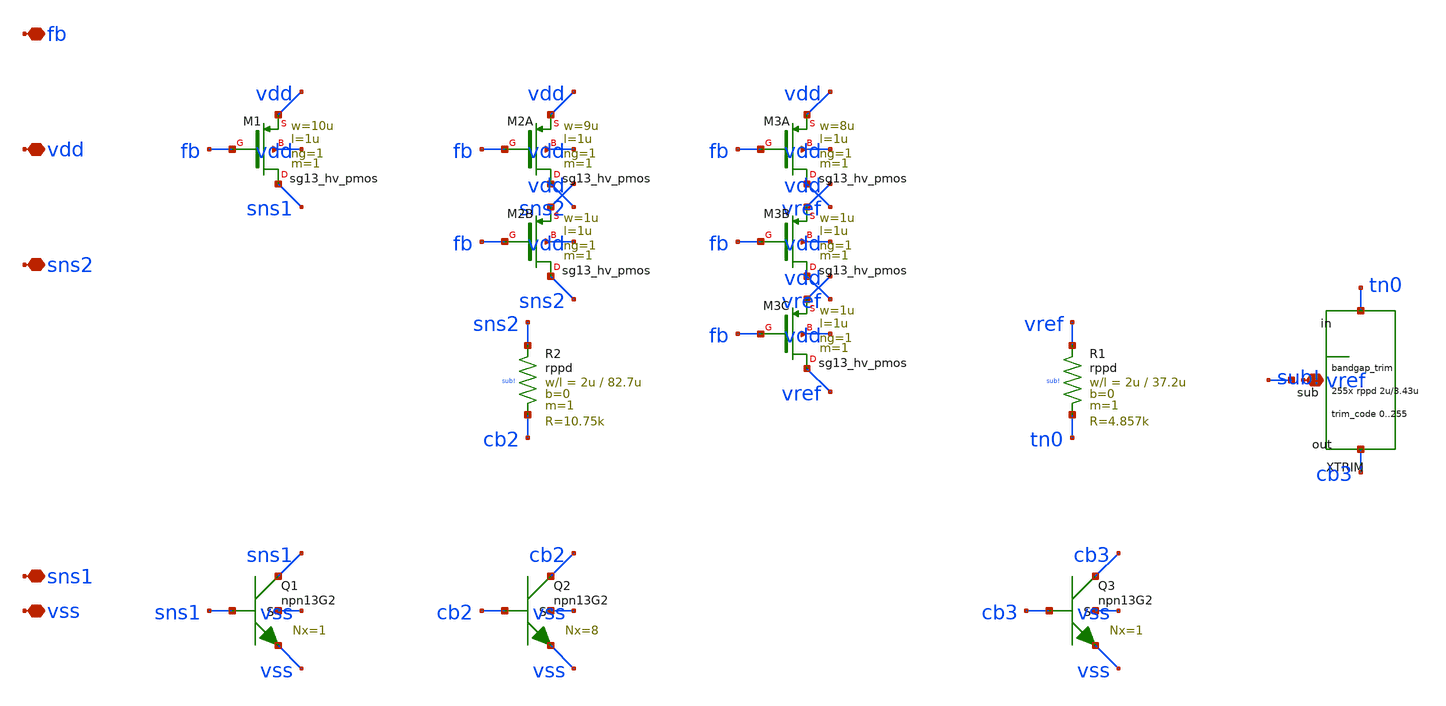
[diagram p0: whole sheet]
** sch_path: design/bandgap_core.sch
**.subckt bandgap_core vdd vss fb sns1 sns2 vref
*.iopin vdd
*.iopin vss
*.iopin fb
*.iopin sns1
*.iopin sns2
*.iopin vref
XM1 sns1 fb vdd vdd sg13_hv_pmos w=10u l=1u ng=1 m=1 mm_ok=1
XQ1 sns1 sns1 vss vss npn13G2 Nx=1 mm_ok=1
XM2A sns2 fb vdd vdd sg13_hv_pmos w=9u l=1u ng=1 m=1 mm_ok=1
XM2B sns2 fb vdd vdd sg13_hv_pmos w=1u l=1u ng=1 m=1 mm_ok=1
XR2 sns2 cb2 sub! rppd w=2u l=82.7u m=1 b=0 mm_ok=1
XQ2 cb2 cb2 vss vss npn13G2 Nx=8 mm_ok=1
XM3A vref fb vdd vdd sg13_hv_pmos w=8u l=1u ng=1 m=1 mm_ok=1
XM3B vref fb vdd vdd sg13_hv_pmos w=1u l=1u ng=1 m=1 mm_ok=1
XM3C vref fb vdd vdd sg13_hv_pmos w=1u l=1u ng=1 m=1 mm_ok=1
XR1 vref tn0 sub! rppd w=2u l=37.2u m=1 b=0 mm_ok=1
XXTRIM tn0 cb3 sub! bandgap_trim
XQ3 cb3 cb3 vss vss npn13G2 Nx=1 mm_ok=1
**.ends

* expanding   symbol:  bandgap_trim.sym # of pins=3
** sym_path: design/bandgap_trim.sym
** sch_path: design/bandgap_trim.sch
.subckt bandgap_trim in out sub

*.iopin in
*.iopin out
*.iopin sub
XRU1 in t001 sub rppd w=2u l=3.43u m=1 b=0 mm_ok=1
XRU2 t001 t002 sub rppd w=2u l=3.43u m=1 b=0 mm_ok=1
XRU3 t002 t003 sub rppd w=2u l=3.43u m=1 b=0 mm_ok=1
XRU4 t003 t004 sub rppd w=2u l=3.43u m=1 b=0 mm_ok=1
XRU5 t004 t005 sub rppd w=2u l=3.43u m=1 b=0 mm_ok=1
XRU6 t005 t006 sub rppd w=2u l=3.43u m=1 b=0 mm_ok=1
XRU7 t006 t007 sub rppd w=2u l=3.43u m=1 b=0 mm_ok=1
XRU8 t007 t008 sub rppd w=2u l=3.43u m=1 b=0 mm_ok=1
XRU9 t008 t009 sub rppd w=2u l=3.43u m=1 b=0 mm_ok=1
XRU10 t009 t010 sub rppd w=2u l=3.43u m=1 b=0 mm_ok=1
XRU11 t010 t011 sub rppd w=2u l=3.43u m=1 b=0 mm_ok=1
XRU12 t011 t012 sub rppd w=2u l=3.43u m=1 b=0 mm_ok=1
XRU13 t012 t013 sub rppd w=2u l=3.43u m=1 b=0 mm_ok=1
XRU14 t013 t014 sub rppd w=2u l=3.43u m=1 b=0 mm_ok=1
XRU15 t014 t015 sub rppd w=2u l=3.43u m=1 b=0 mm_ok=1
XRU16 t015 t016 sub rppd w=2u l=3.43u m=1 b=0 mm_ok=1
XRU17 t016 t017 sub rppd w=2u l=3.43u m=1 b=0 mm_ok=1
XRU18 t017 t018 sub rppd w=2u l=3.43u m=1 b=0 mm_ok=1
XRU19 t018 t019 sub rppd w=2u l=3.43u m=1 b=0 mm_ok=1
XRU20 t019 t020 sub rppd w=2u l=3.43u m=1 b=0 mm_ok=1
XRU21 t020 t021 sub rppd w=2u l=3.43u m=1 b=0 mm_ok=1
XRU22 t021 t022 sub rppd w=2u l=3.43u m=1 b=0 mm_ok=1
XRU23 t022 t023 sub rppd w=2u l=3.43u m=1 b=0 mm_ok=1
XRU24 t023 t024 sub rppd w=2u l=3.43u m=1 b=0 mm_ok=1
XRU25 t024 t025 sub rppd w=2u l=3.43u m=1 b=0 mm_ok=1
XRU26 t025 t026 sub rppd w=2u l=3.43u m=1 b=0 mm_ok=1
XRU27 t026 t027 sub rppd w=2u l=3.43u m=1 b=0 mm_ok=1
XRU28 t027 t028 sub rppd w=2u l=3.43u m=1 b=0 mm_ok=1
XRU29 t028 t029 sub rppd w=2u l=3.43u m=1 b=0 mm_ok=1
XRU30 t029 t030 sub rppd w=2u l=3.43u m=1 b=0 mm_ok=1
XRU31 t030 t031 sub rppd w=2u l=3.43u m=1 b=0 mm_ok=1
XRU32 t031 t032 sub rppd w=2u l=3.43u m=1 b=0 mm_ok=1
XRU33 t032 t033 sub rppd w=2u l=3.43u m=1 b=0 mm_ok=1
XRU34 t033 t034 sub rppd w=2u l=3.43u m=1 b=0 mm_ok=1
XRU35 t034 t035 sub rppd w=2u l=3.43u m=1 b=0 mm_ok=1
XRU36 t035 t036 sub rppd w=2u l=3.43u m=1 b=0 mm_ok=1
XRU37 t036 t037 sub rppd w=2u l=3.43u m=1 b=0 mm_ok=1
XRU38 t037 t038 sub rppd w=2u l=3.43u m=1 b=0 mm_ok=1
XRU39 t038 t039 sub rppd w=2u l=3.43u m=1 b=0 mm_ok=1
XRU40 t039 t040 sub rppd w=2u l=3.43u m=1 b=0 mm_ok=1
XRU41 t040 t041 sub rppd w=2u l=3.43u m=1 b=0 mm_ok=1
XRU42 t041 t042 sub rppd w=2u l=3.43u m=1 b=0 mm_ok=1
XRU43 t042 t043 sub rppd w=2u l=3.43u m=1 b=0 mm_ok=1
XRU44 t043 t044 sub rppd w=2u l=3.43u m=1 b=0 mm_ok=1
XRU45 t044 t045 sub rppd w=2u l=3.43u m=1 b=0 mm_ok=1
XRU46 t045 t046 sub rppd w=2u l=3.43u m=1 b=0 mm_ok=1
XRU47 t046 t047 sub rppd w=2u l=3.43u m=1 b=0 mm_ok=1
XRU48 t047 t048 sub rppd w=2u l=3.43u m=1 b=0 mm_ok=1
XRU49 t048 t049 sub rppd w=2u l=3.43u m=1 b=0 mm_ok=1
XRU50 t049 t050 sub rppd w=2u l=3.43u m=1 b=0 mm_ok=1
XRU51 t050 t051 sub rppd w=2u l=3.43u m=1 b=0 mm_ok=1
XRU52 t051 t052 sub rppd w=2u l=3.43u m=1 b=0 mm_ok=1
XRU53 t052 t053 sub rppd w=2u l=3.43u m=1 b=0 mm_ok=1
XRU54 t053 t054 sub rppd w=2u l=3.43u m=1 b=0 mm_ok=1
XRU55 t054 t055 sub rppd w=2u l=3.43u m=1 b=0 mm_ok=1
XRU56 t055 t056 sub rppd w=2u l=3.43u m=1 b=0 mm_ok=1
XRU57 t056 t057 sub rppd w=2u l=3.43u m=1 b=0 mm_ok=1
XRU58 t057 t058 sub rppd w=2u l=3.43u m=1 b=0 mm_ok=1
XRU59 t058 t059 sub rppd w=2u l=3.43u m=1 b=0 mm_ok=1
XRU60 t059 t060 sub rppd w=2u l=3.43u m=1 b=0 mm_ok=1
XRU61 t060 t061 sub rppd w=2u l=3.43u m=1 b=0 mm_ok=1
XRU62 t061 t062 sub rppd w=2u l=3.43u m=1 b=0 mm_ok=1
XRU63 t062 t063 sub rppd w=2u l=3.43u m=1 b=0 mm_ok=1
XRU64 t063 t064 sub rppd w=2u l=3.43u m=1 b=0 mm_ok=1
XRU65 t064 t065 sub rppd w=2u l=3.43u m=1 b=0 mm_ok=1
XRU66 t065 t066 sub rppd w=2u l=3.43u m=1 b=0 mm_ok=1
XRU67 t066 t067 sub rppd w=2u l=3.43u m=1 b=0 mm_ok=1
XRU68 t067 t068 sub rppd w=2u l=3.43u m=1 b=0 mm_ok=1
XRU69 t068 t069 sub rppd w=2u l=3.43u m=1 b=0 mm_ok=1
XRU70 t069 t070 sub rppd w=2u l=3.43u m=1 b=0 mm_ok=1
XRU71 t070 t071 sub rppd w=2u l=3.43u m=1 b=0 mm_ok=1
XRU72 t071 t072 sub rppd w=2u l=3.43u m=1 b=0 mm_ok=1
XRU73 t072 t073 sub rppd w=2u l=3.43u m=1 b=0 mm_ok=1
XRU74 t073 t074 sub rppd w=2u l=3.43u m=1 b=0 mm_ok=1
XRU75 t074 t075 sub rppd w=2u l=3.43u m=1 b=0 mm_ok=1
XRU76 t075 t076 sub rppd w=2u l=3.43u m=1 b=0 mm_ok=1
XRU77 t076 t077 sub rppd w=2u l=3.43u m=1 b=0 mm_ok=1
XRU78 t077 t078 sub rppd w=2u l=3.43u m=1 b=0 mm_ok=1
XRU79 t078 t079 sub rppd w=2u l=3.43u m=1 b=0 mm_ok=1
XRU80 t079 t080 sub rppd w=2u l=3.43u m=1 b=0 mm_ok=1
XRU81 t080 t081 sub rppd w=2u l=3.43u m=1 b=0 mm_ok=1
XRU82 t081 t082 sub rppd w=2u l=3.43u m=1 b=0 mm_ok=1
XRU83 t082 t083 sub rppd w=2u l=3.43u m=1 b=0 mm_ok=1
XRU84 t083 t084 sub rppd w=2u l=3.43u m=1 b=0 mm_ok=1
XRU85 t084 t085 sub rppd w=2u l=3.43u m=1 b=0 mm_ok=1
XRU86 t085 t086 sub rppd w=2u l=3.43u m=1 b=0 mm_ok=1
XRU87 t086 t087 sub rppd w=2u l=3.43u m=1 b=0 mm_ok=1
XRU88 t087 t088 sub rppd w=2u l=3.43u m=1 b=0 mm_ok=1
XRU89 t088 t089 sub rppd w=2u l=3.43u m=1 b=0 mm_ok=1
XRU90 t089 t090 sub rppd w=2u l=3.43u m=1 b=0 mm_ok=1
XRU91 t090 t091 sub rppd w=2u l=3.43u m=1 b=0 mm_ok=1
XRU92 t091 t092 sub rppd w=2u l=3.43u m=1 b=0 mm_ok=1
XRU93 t092 t093 sub rppd w=2u l=3.43u m=1 b=0 mm_ok=1
XRU94 t093 t094 sub rppd w=2u l=3.43u m=1 b=0 mm_ok=1
XRU95 t094 t095 sub rppd w=2u l=3.43u m=1 b=0 mm_ok=1
XRU96 t095 t096 sub rppd w=2u l=3.43u m=1 b=0 mm_ok=1
XRU97 t096 t097 sub rppd w=2u l=3.43u m=1 b=0 mm_ok=1
XRU98 t097 t098 sub rppd w=2u l=3.43u m=1 b=0 mm_ok=1
XRU99 t098 t099 sub rppd w=2u l=3.43u m=1 b=0 mm_ok=1
XRU100 t099 t100 sub rppd w=2u l=3.43u m=1 b=0 mm_ok=1
XRU101 t100 t101 sub rppd w=2u l=3.43u m=1 b=0 mm_ok=1
XRU102 t101 t102 sub rppd w=2u l=3.43u m=1 b=0 mm_ok=1
XRU103 t102 t103 sub rppd w=2u l=3.43u m=1 b=0 mm_ok=1
XRU104 t103 t104 sub rppd w=2u l=3.43u m=1 b=0 mm_ok=1
XRU105 t104 t105 sub rppd w=2u l=3.43u m=1 b=0 mm_ok=1
XRU106 t105 t106 sub rppd w=2u l=3.43u m=1 b=0 mm_ok=1
XRU107 t106 t107 sub rppd w=2u l=3.43u m=1 b=0 mm_ok=1
XRU108 t107 t108 sub rppd w=2u l=3.43u m=1 b=0 mm_ok=1
XRU109 t108 t109 sub rppd w=2u l=3.43u m=1 b=0 mm_ok=1
XRU110 t109 t110 sub rppd w=2u l=3.43u m=1 b=0 mm_ok=1
XRU111 t110 t111 sub rppd w=2u l=3.43u m=1 b=0 mm_ok=1
XRU112 t111 t112 sub rppd w=2u l=3.43u m=1 b=0 mm_ok=1
XRU113 t112 t113 sub rppd w=2u l=3.43u m=1 b=0 mm_ok=1
XRU114 t113 t114 sub rppd w=2u l=3.43u m=1 b=0 mm_ok=1
XRU115 t114 t115 sub rppd w=2u l=3.43u m=1 b=0 mm_ok=1
XRU116 t115 t116 sub rppd w=2u l=3.43u m=1 b=0 mm_ok=1
XRU117 t116 t117 sub rppd w=2u l=3.43u m=1 b=0 mm_ok=1
XRU118 t117 t118 sub rppd w=2u l=3.43u m=1 b=0 mm_ok=1
XRU119 t118 t119 sub rppd w=2u l=3.43u m=1 b=0 mm_ok=1
XRU120 t119 t120 sub rppd w=2u l=3.43u m=1 b=0 mm_ok=1
XRU121 t120 t121 sub rppd w=2u l=3.43u m=1 b=0 mm_ok=1
XRU122 t121 t122 sub rppd w=2u l=3.43u m=1 b=0 mm_ok=1
XRU123 t122 t123 sub rppd w=2u l=3.43u m=1 b=0 mm_ok=1
XRU124 t123 t124 sub rppd w=2u l=3.43u m=1 b=0 mm_ok=1
XRU125 t124 t125 sub rppd w=2u l=3.43u m=1 b=0 mm_ok=1
XRU126 t125 t126 sub rppd w=2u l=3.43u m=1 b=0 mm_ok=1
XRU127 t126 t127 sub rppd w=2u l=3.43u m=1 b=0 mm_ok=1
XRU128 t127 t128 sub rppd w=2u l=3.43u m=1 b=0 mm_ok=1
XRU129 t128 t129 sub rppd w=2u l=3.43u m=1 b=0 mm_ok=1
XRU130 t129 t130 sub rppd w=2u l=3.43u m=1 b=0 mm_ok=1
XRU131 t130 t131 sub rppd w=2u l=3.43u m=1 b=0 mm_ok=1
XRU132 t131 t132 sub rppd w=2u l=3.43u m=1 b=0 mm_ok=1
XRU133 t132 t133 sub rppd w=2u l=3.43u m=1 b=0 mm_ok=1
XRU134 t133 t134 sub rppd w=2u l=3.43u m=1 b=0 mm_ok=1
XRU135 t134 t135 sub rppd w=2u l=3.43u m=1 b=0 mm_ok=1
XRU136 t135 t136 sub rppd w=2u l=3.43u m=1 b=0 mm_ok=1
XRU137 t136 t137 sub rppd w=2u l=3.43u m=1 b=0 mm_ok=1
XRU138 t137 t138 sub rppd w=2u l=3.43u m=1 b=0 mm_ok=1
XRU139 t138 t139 sub rppd w=2u l=3.43u m=1 b=0 mm_ok=1
XRU140 t139 t140 sub rppd w=2u l=3.43u m=1 b=0 mm_ok=1
XRU141 t140 t141 sub rppd w=2u l=3.43u m=1 b=0 mm_ok=1
XRU142 t141 t142 sub rppd w=2u l=3.43u m=1 b=0 mm_ok=1
XRU143 t142 t143 sub rppd w=2u l=3.43u m=1 b=0 mm_ok=1
XRU144 t143 t144 sub rppd w=2u l=3.43u m=1 b=0 mm_ok=1
XRU145 t144 t145 sub rppd w=2u l=3.43u m=1 b=0 mm_ok=1
XRU146 t145 t146 sub rppd w=2u l=3.43u m=1 b=0 mm_ok=1
XRU147 t146 t147 sub rppd w=2u l=3.43u m=1 b=0 mm_ok=1
XRU148 t147 t148 sub rppd w=2u l=3.43u m=1 b=0 mm_ok=1
XRU149 t148 t149 sub rppd w=2u l=3.43u m=1 b=0 mm_ok=1
XRU150 t149 t150 sub rppd w=2u l=3.43u m=1 b=0 mm_ok=1
XRU151 t150 t151 sub rppd w=2u l=3.43u m=1 b=0 mm_ok=1
XRU152 t151 t152 sub rppd w=2u l=3.43u m=1 b=0 mm_ok=1
XRU153 t152 t153 sub rppd w=2u l=3.43u m=1 b=0 mm_ok=1
XRU154 t153 t154 sub rppd w=2u l=3.43u m=1 b=0 mm_ok=1
XRU155 t154 t155 sub rppd w=2u l=3.43u m=1 b=0 mm_ok=1
XRU156 t155 t156 sub rppd w=2u l=3.43u m=1 b=0 mm_ok=1
XRU157 t156 t157 sub rppd w=2u l=3.43u m=1 b=0 mm_ok=1
XRU158 t157 t158 sub rppd w=2u l=3.43u m=1 b=0 mm_ok=1
XRU159 t158 t159 sub rppd w=2u l=3.43u m=1 b=0 mm_ok=1
XRU160 t159 t160 sub rppd w=2u l=3.43u m=1 b=0 mm_ok=1
XRU161 t160 t161 sub rppd w=2u l=3.43u m=1 b=0 mm_ok=1
XRU162 t161 t162 sub rppd w=2u l=3.43u m=1 b=0 mm_ok=1
XRU163 t162 t163 sub rppd w=2u l=3.43u m=1 b=0 mm_ok=1
XRU164 t163 t164 sub rppd w=2u l=3.43u m=1 b=0 mm_ok=1
XRU165 t164 t165 sub rppd w=2u l=3.43u m=1 b=0 mm_ok=1
XRU166 t165 t166 sub rppd w=2u l=3.43u m=1 b=0 mm_ok=1
XRU167 t166 t167 sub rppd w=2u l=3.43u m=1 b=0 mm_ok=1
XRU168 t167 t168 sub rppd w=2u l=3.43u m=1 b=0 mm_ok=1
XRU169 t168 t169 sub rppd w=2u l=3.43u m=1 b=0 mm_ok=1
XRU170 t169 t170 sub rppd w=2u l=3.43u m=1 b=0 mm_ok=1
XRU171 t170 t171 sub rppd w=2u l=3.43u m=1 b=0 mm_ok=1
XRU172 t171 t172 sub rppd w=2u l=3.43u m=1 b=0 mm_ok=1
XRU173 t172 t173 sub rppd w=2u l=3.43u m=1 b=0 mm_ok=1
XRU174 t173 t174 sub rppd w=2u l=3.43u m=1 b=0 mm_ok=1
XRU175 t174 t175 sub rppd w=2u l=3.43u m=1 b=0 mm_ok=1
XRU176 t175 t176 sub rppd w=2u l=3.43u m=1 b=0 mm_ok=1
XRU177 t176 t177 sub rppd w=2u l=3.43u m=1 b=0 mm_ok=1
XRU178 t177 t178 sub rppd w=2u l=3.43u m=1 b=0 mm_ok=1
XRU179 t178 t179 sub rppd w=2u l=3.43u m=1 b=0 mm_ok=1
XRU180 t179 t180 sub rppd w=2u l=3.43u m=1 b=0 mm_ok=1
XRU181 t180 t181 sub rppd w=2u l=3.43u m=1 b=0 mm_ok=1
XRU182 t181 t182 sub rppd w=2u l=3.43u m=1 b=0 mm_ok=1
XRU183 t182 t183 sub rppd w=2u l=3.43u m=1 b=0 mm_ok=1
XRU184 t183 t184 sub rppd w=2u l=3.43u m=1 b=0 mm_ok=1
XRU185 t184 t185 sub rppd w=2u l=3.43u m=1 b=0 mm_ok=1
XRU186 t185 t186 sub rppd w=2u l=3.43u m=1 b=0 mm_ok=1
XRU187 t186 t187 sub rppd w=2u l=3.43u m=1 b=0 mm_ok=1
XRU188 t187 t188 sub rppd w=2u l=3.43u m=1 b=0 mm_ok=1
XRU189 t188 t189 sub rppd w=2u l=3.43u m=1 b=0 mm_ok=1
XRU190 t189 t190 sub rppd w=2u l=3.43u m=1 b=0 mm_ok=1
XRU191 t190 t191 sub rppd w=2u l=3.43u m=1 b=0 mm_ok=1
XRU192 t191 t192 sub rppd w=2u l=3.43u m=1 b=0 mm_ok=1
XRU193 t192 t193 sub rppd w=2u l=3.43u m=1 b=0 mm_ok=1
XRU194 t193 t194 sub rppd w=2u l=3.43u m=1 b=0 mm_ok=1
XRU195 t194 t195 sub rppd w=2u l=3.43u m=1 b=0 mm_ok=1
XRU196 t195 t196 sub rppd w=2u l=3.43u m=1 b=0 mm_ok=1
XRU197 t196 t197 sub rppd w=2u l=3.43u m=1 b=0 mm_ok=1
XRU198 t197 t198 sub rppd w=2u l=3.43u m=1 b=0 mm_ok=1
XRU199 t198 t199 sub rppd w=2u l=3.43u m=1 b=0 mm_ok=1
XRU200 t199 t200 sub rppd w=2u l=3.43u m=1 b=0 mm_ok=1
XRU201 t200 t201 sub rppd w=2u l=3.43u m=1 b=0 mm_ok=1
XRU202 t201 t202 sub rppd w=2u l=3.43u m=1 b=0 mm_ok=1
XRU203 t202 t203 sub rppd w=2u l=3.43u m=1 b=0 mm_ok=1
XRU204 t203 t204 sub rppd w=2u l=3.43u m=1 b=0 mm_ok=1
XRU205 t204 t205 sub rppd w=2u l=3.43u m=1 b=0 mm_ok=1
XRU206 t205 t206 sub rppd w=2u l=3.43u m=1 b=0 mm_ok=1
XRU207 t206 t207 sub rppd w=2u l=3.43u m=1 b=0 mm_ok=1
XRU208 t207 t208 sub rppd w=2u l=3.43u m=1 b=0 mm_ok=1
XRU209 t208 t209 sub rppd w=2u l=3.43u m=1 b=0 mm_ok=1
XRU210 t209 t210 sub rppd w=2u l=3.43u m=1 b=0 mm_ok=1
XRU211 t210 t211 sub rppd w=2u l=3.43u m=1 b=0 mm_ok=1
XRU212 t211 t212 sub rppd w=2u l=3.43u m=1 b=0 mm_ok=1
XRU213 t212 t213 sub rppd w=2u l=3.43u m=1 b=0 mm_ok=1
XRU214 t213 t214 sub rppd w=2u l=3.43u m=1 b=0 mm_ok=1
XRU215 t214 t215 sub rppd w=2u l=3.43u m=1 b=0 mm_ok=1
XRU216 t215 t216 sub rppd w=2u l=3.43u m=1 b=0 mm_ok=1
XRU217 t216 t217 sub rppd w=2u l=3.43u m=1 b=0 mm_ok=1
XRU218 t217 t218 sub rppd w=2u l=3.43u m=1 b=0 mm_ok=1
XRU219 t218 t219 sub rppd w=2u l=3.43u m=1 b=0 mm_ok=1
XRU220 t219 t220 sub rppd w=2u l=3.43u m=1 b=0 mm_ok=1
XRU221 t220 t221 sub rppd w=2u l=3.43u m=1 b=0 mm_ok=1
XRU222 t221 t222 sub rppd w=2u l=3.43u m=1 b=0 mm_ok=1
XRU223 t222 t223 sub rppd w=2u l=3.43u m=1 b=0 mm_ok=1
XRU224 t223 t224 sub rppd w=2u l=3.43u m=1 b=0 mm_ok=1
XRU225 t224 t225 sub rppd w=2u l=3.43u m=1 b=0 mm_ok=1
XRU226 t225 t226 sub rppd w=2u l=3.43u m=1 b=0 mm_ok=1
XRU227 t226 t227 sub rppd w=2u l=3.43u m=1 b=0 mm_ok=1
XRU228 t227 t228 sub rppd w=2u l=3.43u m=1 b=0 mm_ok=1
XRU229 t228 t229 sub rppd w=2u l=3.43u m=1 b=0 mm_ok=1
XRU230 t229 t230 sub rppd w=2u l=3.43u m=1 b=0 mm_ok=1
XRU231 t230 t231 sub rppd w=2u l=3.43u m=1 b=0 mm_ok=1
XRU232 t231 t232 sub rppd w=2u l=3.43u m=1 b=0 mm_ok=1
XRU233 t232 t233 sub rppd w=2u l=3.43u m=1 b=0 mm_ok=1
XRU234 t233 t234 sub rppd w=2u l=3.43u m=1 b=0 mm_ok=1
XRU235 t234 t235 sub rppd w=2u l=3.43u m=1 b=0 mm_ok=1
XRU236 t235 t236 sub rppd w=2u l=3.43u m=1 b=0 mm_ok=1
XRU237 t236 t237 sub rppd w=2u l=3.43u m=1 b=0 mm_ok=1
XRU238 t237 t238 sub rppd w=2u l=3.43u m=1 b=0 mm_ok=1
XRU239 t238 t239 sub rppd w=2u l=3.43u m=1 b=0 mm_ok=1
XRU240 t239 t240 sub rppd w=2u l=3.43u m=1 b=0 mm_ok=1
XRU241 t240 t241 sub rppd w=2u l=3.43u m=1 b=0 mm_ok=1
XRU242 t241 t242 sub rppd w=2u l=3.43u m=1 b=0 mm_ok=1
XRU243 t242 t243 sub rppd w=2u l=3.43u m=1 b=0 mm_ok=1
XRU244 t243 t244 sub rppd w=2u l=3.43u m=1 b=0 mm_ok=1
XRU245 t244 t245 sub rppd w=2u l=3.43u m=1 b=0 mm_ok=1
XRU246 t245 t246 sub rppd w=2u l=3.43u m=1 b=0 mm_ok=1
XRU247 t246 t247 sub rppd w=2u l=3.43u m=1 b=0 mm_ok=1
XRU248 t247 t248 sub rppd w=2u l=3.43u m=1 b=0 mm_ok=1
XRU249 t248 t249 sub rppd w=2u l=3.43u m=1 b=0 mm_ok=1
XRU250 t249 t250 sub rppd w=2u l=3.43u m=1 b=0 mm_ok=1
XRU251 t250 t251 sub rppd w=2u l=3.43u m=1 b=0 mm_ok=1
XRU252 t251 t252 sub rppd w=2u l=3.43u m=1 b=0 mm_ok=1
XRU253 t252 t253 sub rppd w=2u l=3.43u m=1 b=0 mm_ok=1
XRU254 t253 t254 sub rppd w=2u l=3.43u m=1 b=0 mm_ok=1
XRU255 t254 out sub rppd w=2u l=3.43u m=1 b=0 mm_ok=1
RS0 in t001 {1e-3 + 1e12*(floor(trim_code/1)-2*floor(trim_code/2))} m=1
RS1 t001 t003 {1e-3 + 1e12*(floor(trim_code/2)-2*floor(trim_code/4))} m=1
RS2 t003 t007 {1e-3 + 1e12*(floor(trim_code/4)-2*floor(trim_code/8))} m=1
RS3 t007 t015 {1e-3 + 1e12*(floor(trim_code/8)-2*floor(trim_code/16))} m=1
RS4 t015 t031 {1e-3 + 1e12*(floor(trim_code/16)-2*floor(trim_code/32))} m=1
RS5 t031 t063 {1e-3 + 1e12*(floor(trim_code/32)-2*floor(trim_code/64))} m=1
RS6 t063 t127 {1e-3 + 1e12*(floor(trim_code/64)-2*floor(trim_code/128))} m=1
RS7 t127 out {1e-3 + 1e12*(floor(trim_code/128)-2*floor(trim_code/256))} m=1
**** begin user architecture code

.param trim_code=128

**** end user architecture code
.ends

.end
